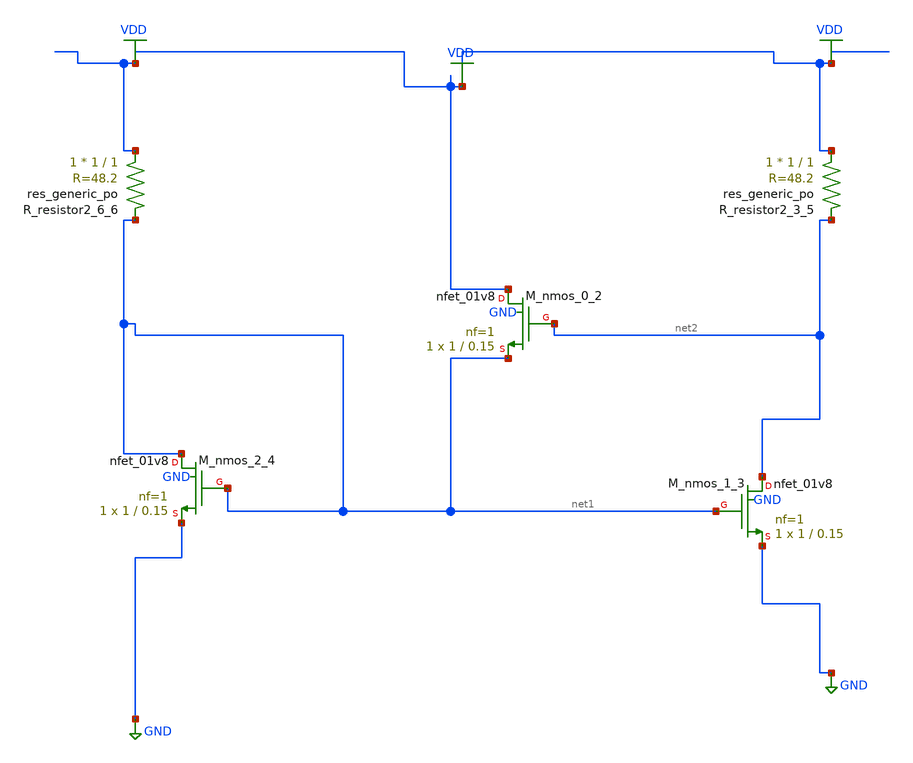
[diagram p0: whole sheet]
** sch_path: schematics/AMSNet/327.sch
**.subckt 327
XM_nmos_0_2 VDD net2 net1 GND sky130_fd_pr__nfet_01v8 L=0.15 W=1 nf=1 ad='int((1 + 1)/2) * 1 / 1 * 0.29'
+ as='int((1 + 2)/2) * 1 / 1 * 0.29' pd='2*int((1 + 1)/2) * (1 / 1 + 0.29)' ps='2*int((1 + 2)/2) * (1 / 1 + 0.29)'
+ nrd='0.29 / 1 ' nrs='0.29 / 1 ' sa=0 sb=0 sd=0 mult=1 m=1
XM_nmos_1_3 net2 net1 GND GND sky130_fd_pr__nfet_01v8 L=0.15 W=1 nf=1 ad='int((1 + 1)/2) * 1 / 1 * 0.29'
+ as='int((1 + 2)/2) * 1 / 1 * 0.29' pd='2*int((1 + 1)/2) * (1 / 1 + 0.29)' ps='2*int((1 + 2)/2) * (1 / 1 + 0.29)'
+ nrd='0.29 / 1 ' nrs='0.29 / 1 ' sa=0 sb=0 sd=0 mult=1 m=1
XM_nmos_2_4 net1 net1 GND GND sky130_fd_pr__nfet_01v8 L=0.15 W=1 nf=1 ad='int((1 + 1)/2) * 1 / 1 * 0.29'
+ as='int((1 + 2)/2) * 1 / 1 * 0.29' pd='2*int((1 + 1)/2) * (1 / 1 + 0.29)' ps='2*int((1 + 2)/2) * (1 / 1 + 0.29)'
+ nrd='0.29 / 1 ' nrs='0.29 / 1 ' sa=0 sb=0 sd=0 mult=1 m=1
XR_resistor2_3_5 VDD net2 sky130_fd_pr__res_generic_po W=1 L=1 m=1
XR_resistor2_6_6 VDD net1 sky130_fd_pr__res_generic_po W=1 L=1 m=1
**.ends
.GLOBAL GND
.GLOBAL VDD
.end
